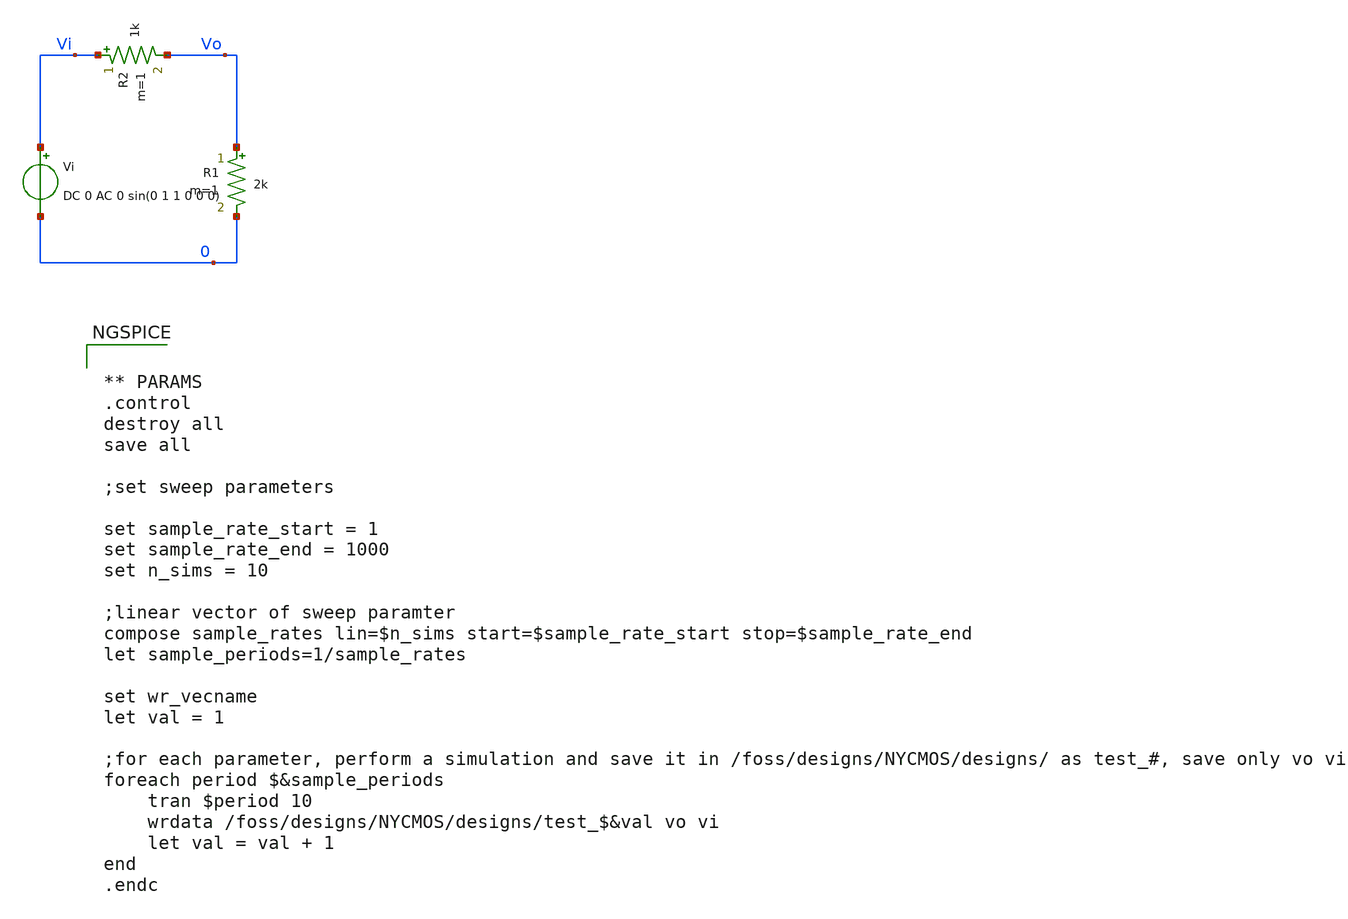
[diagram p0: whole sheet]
** sch_path: designs/simulation_parasitics/schematics/parametric_sim_export_example.sch
**.subckt parametric_sim_export_example
R1 Vo 0 2k m=1
Vi Vi 0 DC 0 AC 0 sin(0 1 1 0 0 0)
R2 Vi Vo 1k m=1
**** begin user architecture code


** PARAMS
.control
destroy all
save all

;set sweep parameters

set sample_rate_start = 1
set sample_rate_end = 1000
set n_sims = 10

;linear vector of sweep paramter
compose sample_rates lin=$n_sims start=$sample_rate_start stop=$sample_rate_end
let sample_periods=1/sample_rates

set wr_vecname
let val = 1

;for each parameter, perform a simulation and save it in /foss/designs/NYCMOS/designs/ as test_#,
+ save only vo vi
foreach period $&sample_periods
	tran $period 10
	wrdata /foss/designs/NYCMOS/designs/test_$&val vo vi
	let val = val + 1
end
.endc


**** end user architecture code
**.ends
.end
